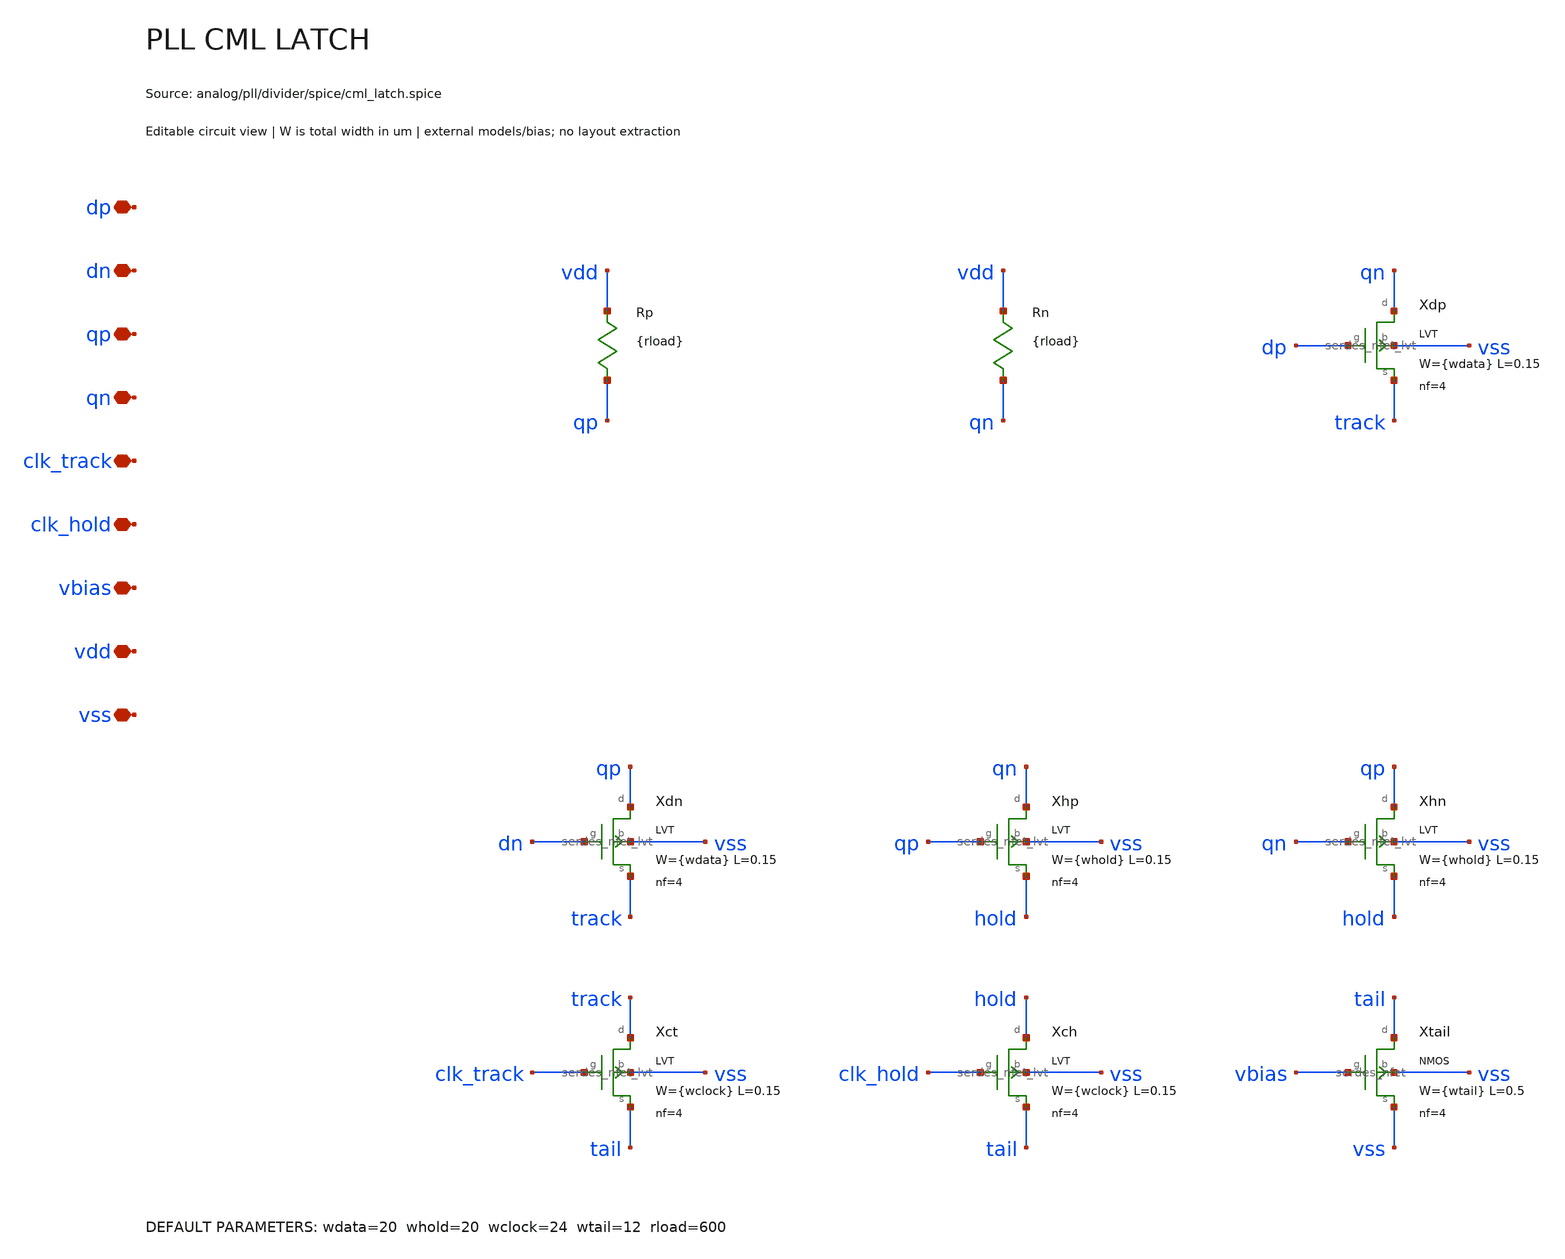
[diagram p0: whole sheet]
** sch_path: analog/pll/divider/schematic/pll_cml_latch.sch
**.subckt pll_cml_latch dp dn qp qn clk_track clk_hold vbias vdd vss
*.iopin dp
*.iopin dn
*.iopin qp
*.iopin qn
*.iopin clk_track
*.iopin clk_hold
*.iopin vbias
*.iopin vdd
*.iopin vss
Rp vdd qp {rload}
Rn vdd qn {rload}
Xdp qn dp track vss serdes_nfet_lvt w={wdata} l=0.15 nf=4
Xdn qp dn track vss serdes_nfet_lvt w={wdata} l=0.15 nf=4
Xhp qn qp hold vss serdes_nfet_lvt w={whold} l=0.15 nf=4
Xhn qp qn hold vss serdes_nfet_lvt w={whold} l=0.15 nf=4
Xct track clk_track tail vss serdes_nfet_lvt w={wclock} l=0.15 nf=4
Xch hold clk_hold tail vss serdes_nfet_lvt w={wclock} l=0.15 nf=4
Xtail tail vbias vss vss serdes_nfet w={wtail} l=0.5 nf=4
**.ends

* expanding   symbol:  serdes/serdes_nfet_lvt.sym # of pins=4
** sym_path: analog/common/devices/schematic/serdes_nfet_lvt.sym
** sch_path: analog/common/devices/schematic/serdes_nfet_lvt.sch
.subckt serdes_nfet_lvt d g s b  w=1 l=0.15 nf=1
*.iopin d
*.iopin g
*.iopin s
*.iopin b
Xmos d g s b sky130_fd_pr__nfet_01v8_lvt w={w} l={l} nf={nf} ad={floor((nf+1)/2)*(w/nf)*0.29} as={floor((nf+2)/2)*(w/nf)*0.29}
+ pd={2*floor((nf+1)/2)*(w/nf+0.29)} ps={2*floor((nf+2)/2)*(w/nf+0.29)}
.ends


* expanding   symbol:  serdes/serdes_nfet.sym # of pins=4
** sym_path: analog/common/devices/schematic/serdes_nfet.sym
** sch_path: analog/common/devices/schematic/serdes_nfet.sch
.subckt serdes_nfet d g s b  w=1 l=0.15 nf=1
*.iopin d
*.iopin g
*.iopin s
*.iopin b
Xmos d g s b sky130_fd_pr__nfet_01v8 w={w} l={l} nf={nf} ad={floor((nf+1)/2)*(w/nf)*0.29} as={floor((nf+2)/2)*(w/nf)*0.29}
+ pd={2*floor((nf+1)/2)*(w/nf+0.29)} ps={2*floor((nf+2)/2)*(w/nf+0.29)}
.ends

.end
